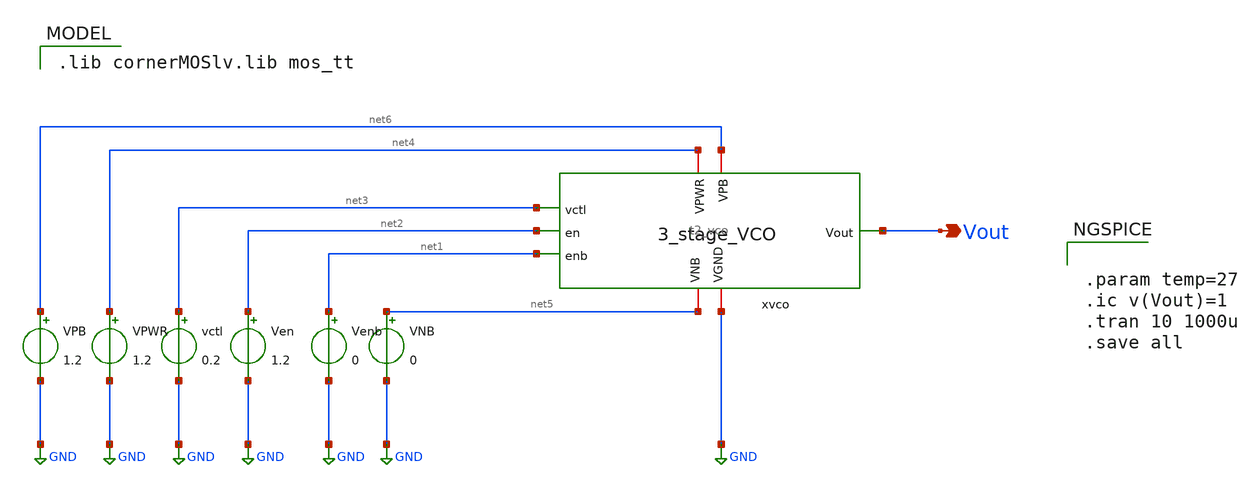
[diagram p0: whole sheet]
** sch_path: Team 2 Design/design_data/xschem/t2_vco_tb.sch
**.subckt t2_vco_tb Vout
*.opin Vout
VPWR net4 GND 1.2
vctl net3 GND 0.2
Ven net2 GND 1.2
Venb net1 GND 0
VNB net5 GND 0
VPB net6 GND 1.2
x1 net4 net6 GND net5 Vout net3 net2 net1 t2_vco
**** begin user architecture code
 .lib cornerMOSlv.lib mos_tt



.param temp=27
.ic v(Vout)=1
.tran 10 1000u
.save all


**** end user architecture code
**.ends

* expanding   symbol:  /foss/designs/cmos-pll-ihp-sg13g2/Team 2 Design/design_data/xschem/t2_vco.sym
*+ # of pins=8
** sym_path: Team 2 Design/design_data/xschem/t2_vco.sym
** sch_path: Team 2 Design/design_data/xschem/t2_vco.sch
.subckt t2_vco VPWR VPB VGND VNB Vout vctl en enb
*.iopin VPWR
*.iopin VPB
*.iopin VGND
*.iopin VNB
*.ipin vctl
*.ipin en
*.ipin enb
*.opin Vout
XM1 net1 en VPWR VPB sg13_lv_pmos w=1.0u l=0.15u ng=1 m=1 mm_ok=1
XM2 net1 net1 VPWR VPB sg13_lv_pmos w=3.0u l=0.15u ng=1 m=1 mm_ok=1
XM3 vco_source net1 VPWR VPB sg13_lv_pmos w=3.0u l=0.15u ng=1 m=1 mm_ok=1
XM4 net1 vctl net2 VNB sg13_lv_nmos w=0.75u l=0.15u ng=1 m=2 mm_ok=1
XM5 net2 net2 VGND VNB sg13_lv_nmos w=1.5u l=0.15u ng=1 m=1 mm_ok=1
XM6 vco_sink net2 VGND VNB sg13_lv_nmos w=1.5u l=0.15u ng=1 m=1 mm_ok=1
XM7 net2 enb VGND VNB sg13_lv_nmos w=0.15u l=0.15u ng=1 m=1 mm_ok=1
XM8 vctl enb VGND VNB sg13_lv_nmos w=0.5u l=0.15u ng=1 m=1 mm_ok=1
XM9 Vout enb VGND VNB sg13_lv_nmos w=0.5u l=0.15u ng=1 m=1 mm_ok=1
x1 vco_source VPB net5 net6 VNB vco_sink t2_vco_inverter
x2 vco_source VPB net7 net8 VNB vco_sink t2_vco_inverter
x3 vco_source VPB net9 net10 VNB vco_sink t2_vco_inverter
.ends


* expanding   symbol:  /foss/designs/cmos-pll-ihp-sg13g2/Team 2
*+ Design/design_data/xschem/t2_vco_inverter.sym # of pins=6
** sym_path: Team 2 Design/design_data/xschem/t2_vco_inverter.sym
** sch_path: Team 2 Design/design_data/xschem/t2_vco_inverter.sch
.subckt t2_vco_inverter VPWR VPB A Y VNB VGND
*.iopin VPWR
*.iopin VGND
*.ipin A
*.opin Y
*.iopin VPB
*.iopin VNB
XM2 Y A VPWR VPB sg13_lv_pmos w=1u l=0.13u ng=1 m=1 mm_ok=1
XM1 Y A VGND VNB sg13_lv_nmos w=0.5u l=0.13u ng=1 m=1 mm_ok=1
.ends

.GLOBAL GND
.end
